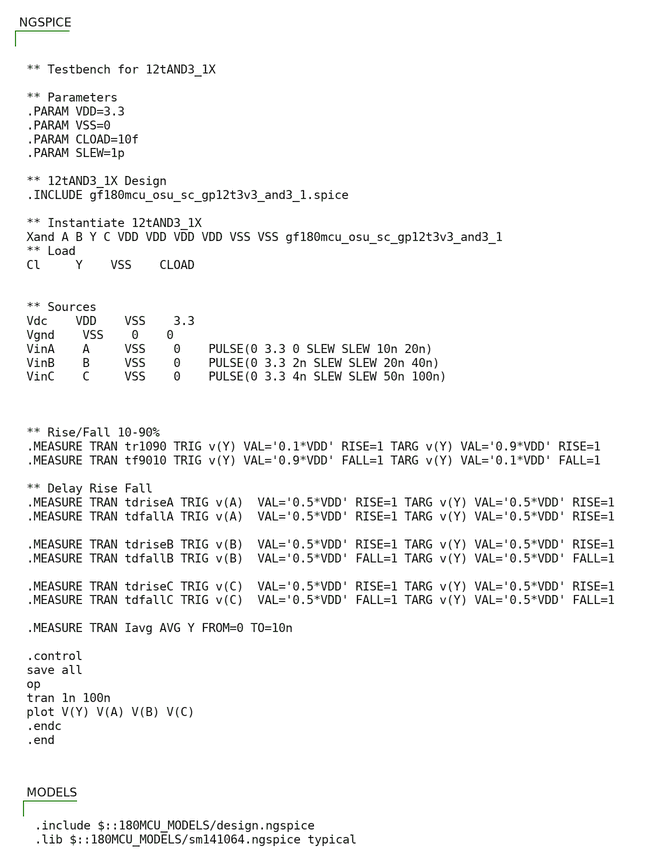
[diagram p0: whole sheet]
** sch_path: designs/libs/core_digital/gf180mcu_osu_sc_gp12t3v3/cells/and3/xschem/TBgf180mcu_osu_sc_gp12t3v3_and3_1.sch
**.subckt TBgf180mcu_osu_sc_gp12t3v3_and3_1
**** begin user architecture code



** Testbench for 12tAND3_1X

** Parameters
.PARAM VDD=3.3
.PARAM VSS=0
.PARAM CLOAD=10f
.PARAM SLEW=1p

** 12tAND3_1X Design
.INCLUDE gf180mcu_osu_sc_gp12t3v3_and3_1.spice

** Instantiate 12tAND3_1X
Xand A B Y C VDD VDD VDD VDD VSS VSS gf180mcu_osu_sc_gp12t3v3_and3_1
** Load
Cl 	Y	VSS	CLOAD


** Sources
Vdc	VDD	VSS	3.3
Vgnd	VSS	0	0
VinA	A 	VSS	0	PULSE(0 3.3 0 SLEW SLEW 10n 20n)
VinB	B 	VSS	0	PULSE(0 3.3 2n SLEW SLEW 20n 40n)
VinC	C 	VSS	0	PULSE(0 3.3 4n SLEW SLEW 50n 100n)



** Rise/Fall 10-90%
.MEASURE TRAN tr1090 TRIG v(Y) VAL='0.1*VDD' RISE=1 TARG v(Y) VAL='0.9*VDD' RISE=1
.MEASURE TRAN tf9010 TRIG v(Y) VAL='0.9*VDD' FALL=1 TARG v(Y) VAL='0.1*VDD' FALL=1

** Delay Rise Fall
.MEASURE TRAN tdriseA TRIG v(A)  VAL='0.5*VDD' RISE=1 TARG v(Y) VAL='0.5*VDD' RISE=1
.MEASURE TRAN tdfallA TRIG v(A)  VAL='0.5*VDD' RISE=1 TARG v(Y) VAL='0.5*VDD' RISE=1

.MEASURE TRAN tdriseB TRIG v(B)  VAL='0.5*VDD' RISE=1 TARG v(Y) VAL='0.5*VDD' RISE=1
.MEASURE TRAN tdfallB TRIG v(B)  VAL='0.5*VDD' FALL=1 TARG v(Y) VAL='0.5*VDD' FALL=1

.MEASURE TRAN tdriseC TRIG v(C)  VAL='0.5*VDD' RISE=1 TARG v(Y) VAL='0.5*VDD' RISE=1
.MEASURE TRAN tdfallC TRIG v(C)  VAL='0.5*VDD' FALL=1 TARG v(Y) VAL='0.5*VDD' FALL=1

.MEASURE TRAN Iavg AVG Y FROM=0 TO=10n

.control
save all
op
tran 1n 100n
plot V(Y) V(A) V(B) V(C)
.endc
.end




.include $::180MCU_MODELS/design.ngspice
.lib $::180MCU_MODELS/sm141064.ngspice typical

**** end user architecture code
**.ends
.end
